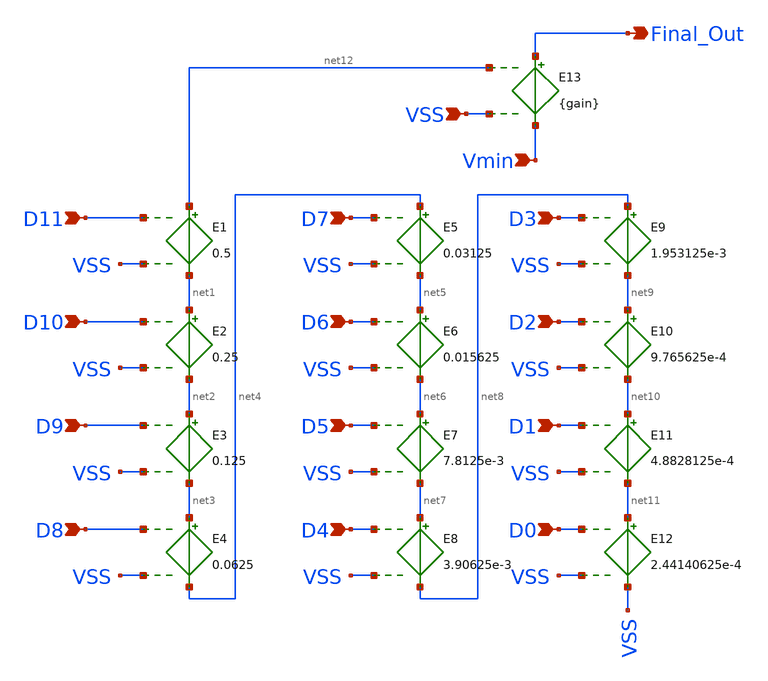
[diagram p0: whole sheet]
** sch_path: DAC_test_ideal.sch
**.subckt DAC_test_ideal D11 D10 D9 D8 D7 D6 D5 D4 D3 D2 D1 D0 Vmin VSS Final_Out
*.ipin D11
*.ipin D10
*.ipin D9
*.ipin D8
*.ipin D7
*.ipin D6
*.ipin D5
*.ipin D4
*.ipin D3
*.ipin D2
*.ipin D1
*.ipin D0
*.ipin Vmin
*.ipin VSS
*.opin Final_Out
E1 net12 net1 D11 VSS 0.5
E2 net1 net2 D10 VSS 0.25
E3 net2 net3 D9 VSS 0.125
E4 net3 net4 D8 VSS 0.0625
E5 net4 net5 D7 VSS 0.03125
E6 net5 net6 D6 VSS 0.015625
E7 net6 net7 D5 VSS 7.8125e-3
E8 net7 net8 D4 VSS 3.90625e-3
E9 net8 net9 D3 VSS 1.953125e-3
E10 net9 net10 D2 VSS 9.765625e-4
E11 net10 net11 D1 VSS 4.8828125e-4
E12 net11 VSS D0 VSS 2.44140625e-4
E13 Final_Out Vmin net12 VSS {gain}
**.ends
.end
